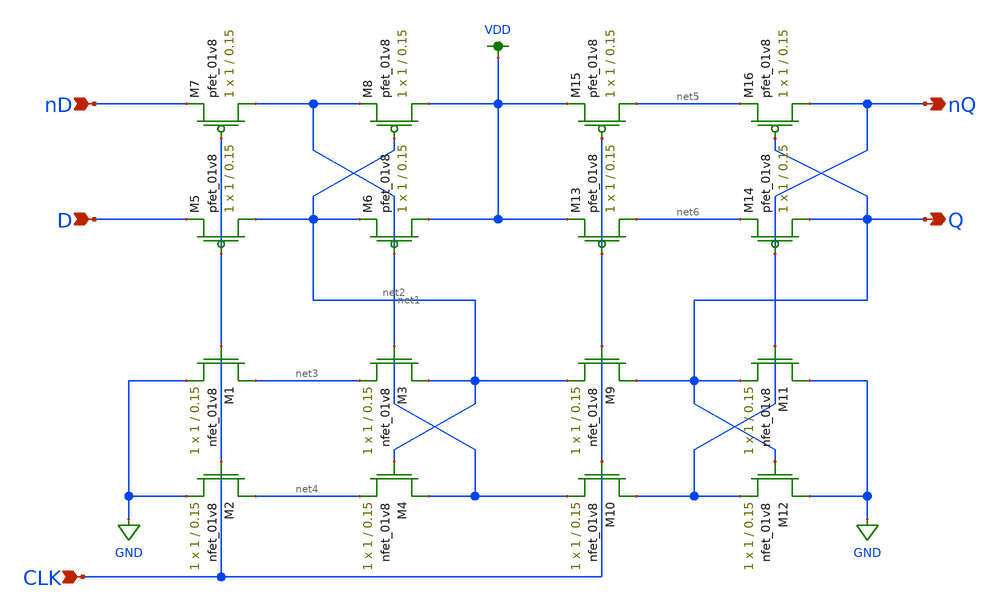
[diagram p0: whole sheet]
** sch_path: mini2/schem/dff_lvs.sch
**.subckt dff_lvs CLK D Q nQ nD
*.ipin CLK
*.ipin D
*.opin Q
*.opin nQ
*.ipin nD
XM1 net3 CLK GND GND sky130_fd_pr__nfet_01v8 L=0.15 W=1 nf=1 ad='int((nf+1)/2) * W/nf * 0.29' as='int((nf+2)/2) * W/nf * 0.29'
+ pd='2*int((nf+1)/2) * (W/nf + 0.29)' ps='2*int((nf+2)/2) * (W/nf + 0.29)' nrd='0.29 / W' nrs='0.29 / W'
+ sa=0 sb=0 sd=0 mult=1 m=1
XM2 net4 CLK GND GND sky130_fd_pr__nfet_01v8 L=0.15 W=1 nf=1 ad='int((nf+1)/2) * W/nf * 0.29' as='int((nf+2)/2) * W/nf * 0.29'
+ pd='2*int((nf+1)/2) * (W/nf + 0.29)' ps='2*int((nf+2)/2) * (W/nf + 0.29)' nrd='0.29 / W' nrs='0.29 / W'
+ sa=0 sb=0 sd=0 mult=1 m=1
XM3 net2 net1 net3 GND sky130_fd_pr__nfet_01v8 L=0.15 W=1 nf=1 ad='int((nf+1)/2) * W/nf * 0.29' as='int((nf+2)/2) * W/nf * 0.29'
+ pd='2*int((nf+1)/2) * (W/nf + 0.29)' ps='2*int((nf+2)/2) * (W/nf + 0.29)' nrd='0.29 / W' nrs='0.29 / W'
+ sa=0 sb=0 sd=0 mult=1 m=1
XM4 net1 net2 net4 GND sky130_fd_pr__nfet_01v8 L=0.15 W=1 nf=1 ad='int((nf+1)/2) * W/nf * 0.29' as='int((nf+2)/2) * W/nf * 0.29'
+ pd='2*int((nf+1)/2) * (W/nf + 0.29)' ps='2*int((nf+2)/2) * (W/nf + 0.29)' nrd='0.29 / W' nrs='0.29 / W'
+ sa=0 sb=0 sd=0 mult=1 m=1
XM5 net2 CLK D VDD sky130_fd_pr__pfet_01v8 L=0.15 W=1 nf=1 ad='int((nf+1)/2) * W/nf * 0.29' as='int((nf+2)/2) * W/nf * 0.29'
+ pd='2*int((nf+1)/2) * (W/nf + 0.29)' ps='2*int((nf+2)/2) * (W/nf + 0.29)' nrd='0.29 / W' nrs='0.29 / W'
+ sa=0 sb=0 sd=0 mult=1 m=1
XM6 VDD net1 net2 VDD sky130_fd_pr__pfet_01v8 L=0.15 W=1 nf=1 ad='int((nf+1)/2) * W/nf * 0.29' as='int((nf+2)/2) * W/nf * 0.29'
+ pd='2*int((nf+1)/2) * (W/nf + 0.29)' ps='2*int((nf+2)/2) * (W/nf + 0.29)' nrd='0.29 / W' nrs='0.29 / W'
+ sa=0 sb=0 sd=0 mult=1 m=1
XM7 net1 CLK nD VDD sky130_fd_pr__pfet_01v8 L=0.15 W=1 nf=1 ad='int((nf+1)/2) * W/nf * 0.29' as='int((nf+2)/2) * W/nf * 0.29'
+ pd='2*int((nf+1)/2) * (W/nf + 0.29)' ps='2*int((nf+2)/2) * (W/nf + 0.29)' nrd='0.29 / W' nrs='0.29 / W'
+ sa=0 sb=0 sd=0 mult=1 m=1
XM8 VDD net2 net1 VDD sky130_fd_pr__pfet_01v8 L=0.15 W=1 nf=1 ad='int((nf+1)/2) * W/nf * 0.29' as='int((nf+2)/2) * W/nf * 0.29'
+ pd='2*int((nf+1)/2) * (W/nf + 0.29)' ps='2*int((nf+2)/2) * (W/nf + 0.29)' nrd='0.29 / W' nrs='0.29 / W'
+ sa=0 sb=0 sd=0 mult=1 m=1
XM9 Q CLK net2 GND sky130_fd_pr__nfet_01v8 L=0.15 W=1 nf=1 ad='int((nf+1)/2) * W/nf * 0.29' as='int((nf+2)/2) * W/nf * 0.29'
+ pd='2*int((nf+1)/2) * (W/nf + 0.29)' ps='2*int((nf+2)/2) * (W/nf + 0.29)' nrd='0.29 / W' nrs='0.29 / W'
+ sa=0 sb=0 sd=0 mult=1 m=1
XM10 nQ CLK net1 GND sky130_fd_pr__nfet_01v8 L=0.15 W=1 nf=1 ad='int((nf+1)/2) * W/nf * 0.29' as='int((nf+2)/2) * W/nf * 0.29'
+ pd='2*int((nf+1)/2) * (W/nf + 0.29)' ps='2*int((nf+2)/2) * (W/nf + 0.29)' nrd='0.29 / W' nrs='0.29 / W'
+ sa=0 sb=0 sd=0 mult=1 m=1
XM11 GND nQ Q GND sky130_fd_pr__nfet_01v8 L=0.15 W=1 nf=1 ad='int((nf+1)/2) * W/nf * 0.29' as='int((nf+2)/2) * W/nf * 0.29'
+ pd='2*int((nf+1)/2) * (W/nf + 0.29)' ps='2*int((nf+2)/2) * (W/nf + 0.29)' nrd='0.29 / W' nrs='0.29 / W'
+ sa=0 sb=0 sd=0 mult=1 m=1
XM12 GND Q nQ GND sky130_fd_pr__nfet_01v8 L=0.15 W=1 nf=1 ad='int((nf+1)/2) * W/nf * 0.29' as='int((nf+2)/2) * W/nf * 0.29'
+ pd='2*int((nf+1)/2) * (W/nf + 0.29)' ps='2*int((nf+2)/2) * (W/nf + 0.29)' nrd='0.29 / W' nrs='0.29 / W'
+ sa=0 sb=0 sd=0 mult=1 m=1
XM13 net6 CLK VDD VDD sky130_fd_pr__pfet_01v8 L=0.15 W=1 nf=1 ad='int((nf+1)/2) * W/nf * 0.29' as='int((nf+2)/2) * W/nf * 0.29'
+ pd='2*int((nf+1)/2) * (W/nf + 0.29)' ps='2*int((nf+2)/2) * (W/nf + 0.29)' nrd='0.29 / W' nrs='0.29 / W'
+ sa=0 sb=0 sd=0 mult=1 m=1
XM14 Q nQ net6 VDD sky130_fd_pr__pfet_01v8 L=0.15 W=1 nf=1 ad='int((nf+1)/2) * W/nf * 0.29' as='int((nf+2)/2) * W/nf * 0.29'
+ pd='2*int((nf+1)/2) * (W/nf + 0.29)' ps='2*int((nf+2)/2) * (W/nf + 0.29)' nrd='0.29 / W' nrs='0.29 / W'
+ sa=0 sb=0 sd=0 mult=1 m=1
XM15 net5 CLK VDD VDD sky130_fd_pr__pfet_01v8 L=0.15 W=1 nf=1 ad='int((nf+1)/2) * W/nf * 0.29' as='int((nf+2)/2) * W/nf * 0.29'
+ pd='2*int((nf+1)/2) * (W/nf + 0.29)' ps='2*int((nf+2)/2) * (W/nf + 0.29)' nrd='0.29 / W' nrs='0.29 / W'
+ sa=0 sb=0 sd=0 mult=1 m=1
XM16 nQ Q net5 VDD sky130_fd_pr__pfet_01v8 L=0.15 W=1 nf=1 ad='int((nf+1)/2) * W/nf * 0.29' as='int((nf+2)/2) * W/nf * 0.29'
+ pd='2*int((nf+1)/2) * (W/nf + 0.29)' ps='2*int((nf+2)/2) * (W/nf + 0.29)' nrd='0.29 / W' nrs='0.29 / W'
+ sa=0 sb=0 sd=0 mult=1 m=1
**.ends
.GLOBAL VDD
.GLOBAL GND
.end
